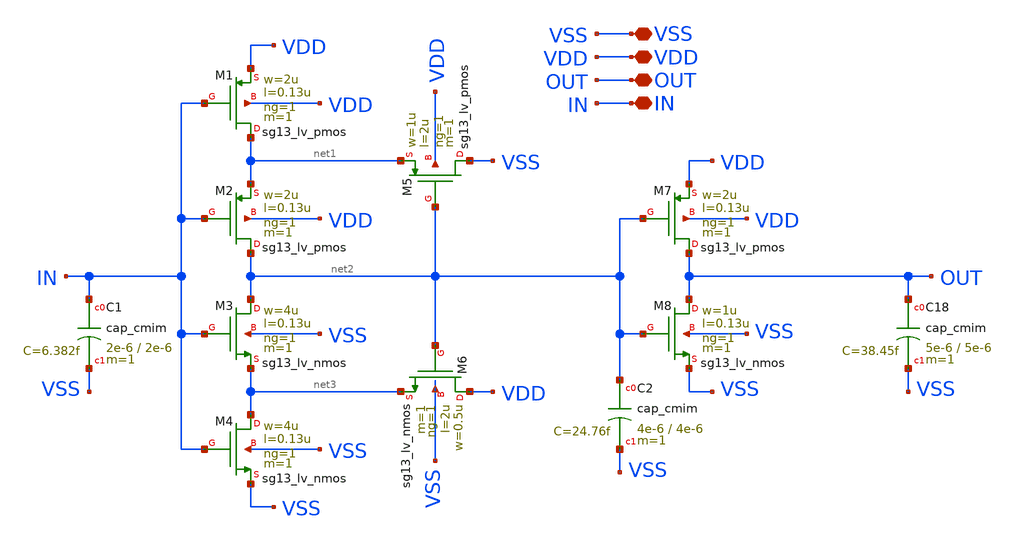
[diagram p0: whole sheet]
** sch_path: xschem/Schmitt_Comparator.sch
**.subckt Schmitt_Comparator VSS VDD OUT IN
*.iopin VSS
*.iopin VDD
*.iopin OUT
*.iopin IN
XM1 net1 IN VDD VDD sg13_lv_pmos w=2u l=0.13u ng=1 m=1 mm_ok=1
XM2 net2 IN net1 VDD sg13_lv_pmos w=2u l=0.13u ng=1 m=1 mm_ok=1
XM3 net2 IN net3 VSS sg13_lv_nmos w=4u l=0.13u ng=1 m=1 mm_ok=1
XM4 net3 IN VSS VSS sg13_lv_nmos w=4u l=0.13u ng=1 m=1 mm_ok=1
XM5 VSS net2 net1 VDD sg13_lv_pmos w=1u l=2u ng=1 m=1 mm_ok=1
XM6 VDD net2 net3 VSS sg13_lv_nmos w=0.5u l=2u ng=1 m=1 mm_ok=1
XC1 IN VSS cap_cmim w=2e-6 l=2e-6 m=1 mm_ok=1
XC18 OUT VSS cap_cmim w=5e-6 l=5e-6 m=1 mm_ok=1
XM7 OUT net2 VDD VDD sg13_lv_pmos w=2u l=0.13u ng=1 m=1 mm_ok=1
XM8 OUT net2 VSS VSS sg13_lv_nmos w=1u l=0.13u ng=1 m=1 mm_ok=1
XC2 net2 VSS cap_cmim w=4e-6 l=4e-6 m=1 mm_ok=1
**.ends
.end
